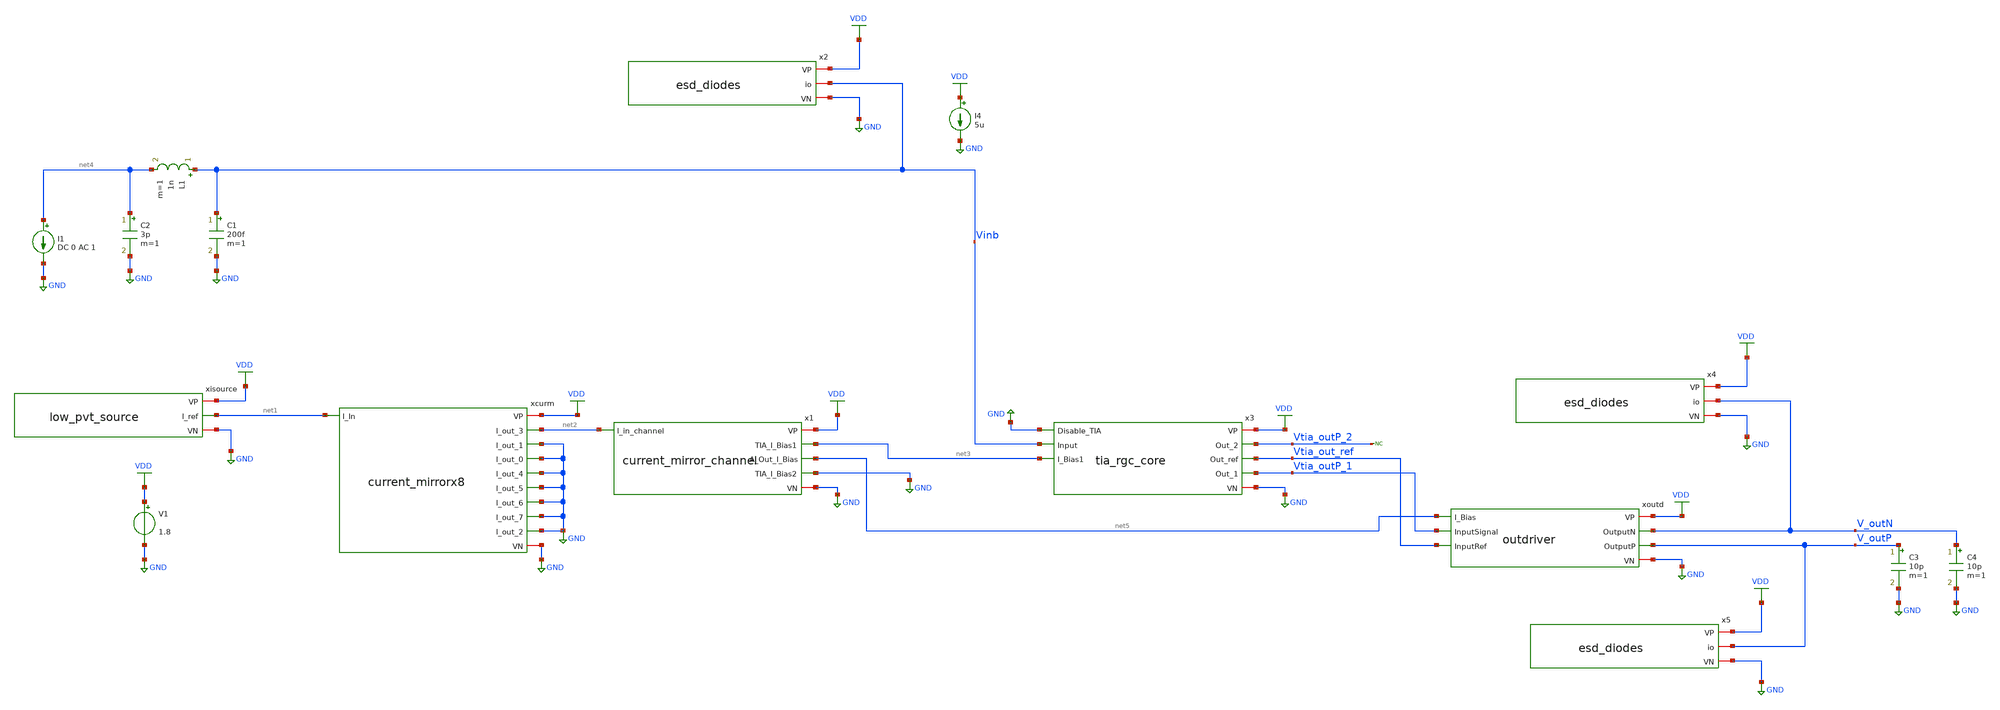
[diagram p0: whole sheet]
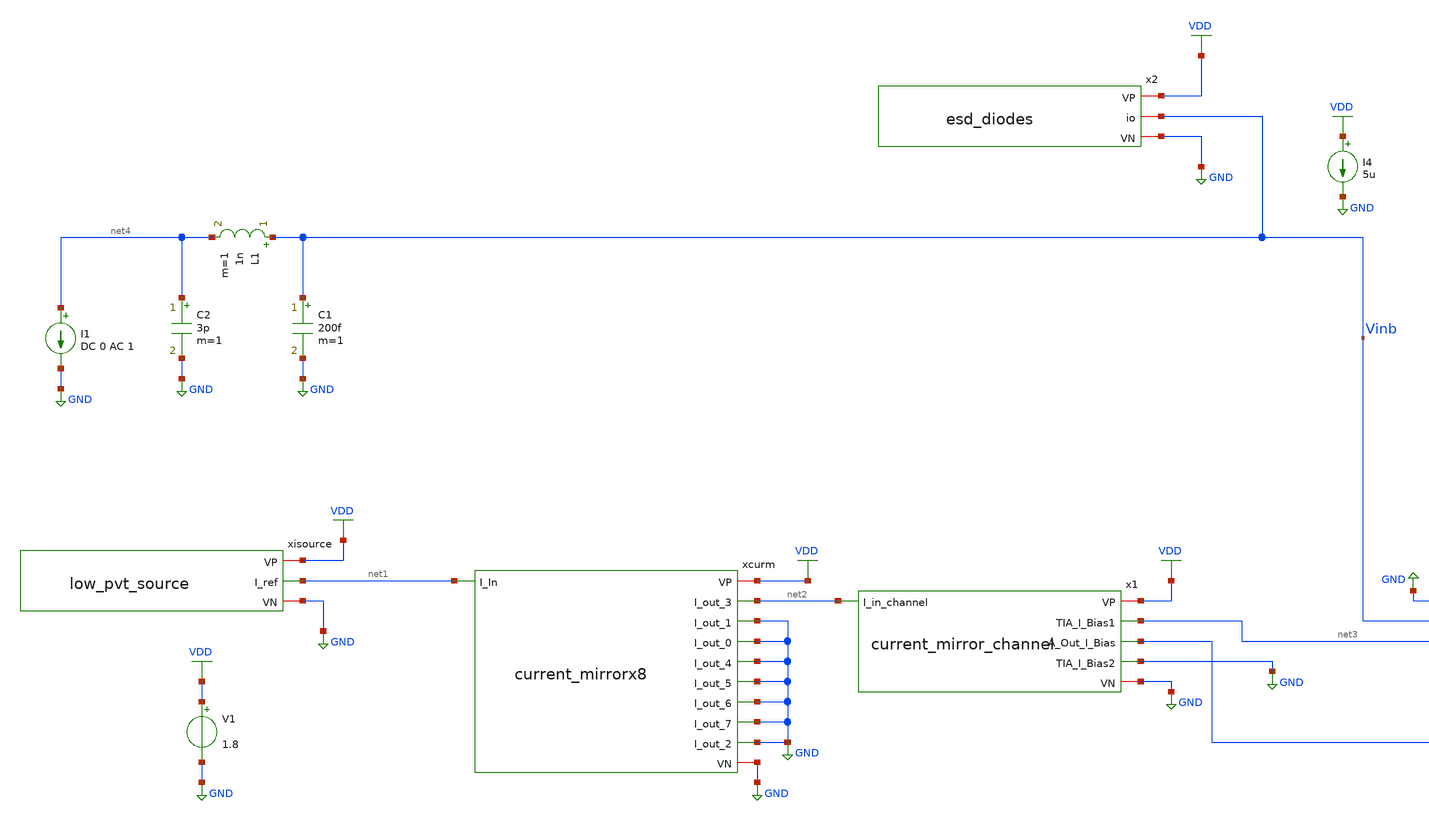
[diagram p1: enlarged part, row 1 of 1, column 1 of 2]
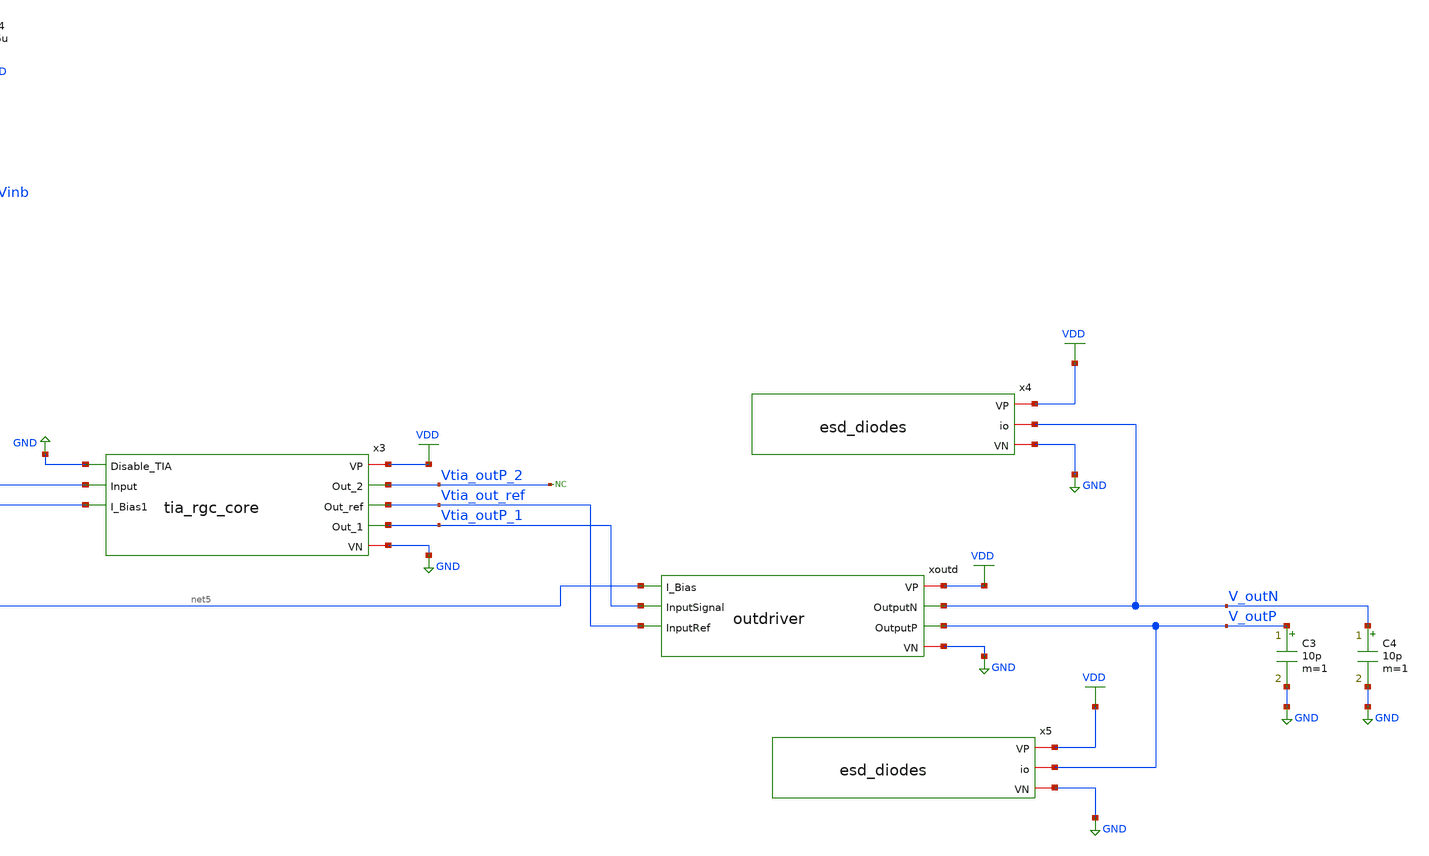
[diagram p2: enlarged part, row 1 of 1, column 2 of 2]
** sch_path: xschem/test/test_tia_rgc_integration.sch
**.subckt test_tia_rgc_integration
xcurm VDD net2 GND net1 GND GND GND GND GND GND GND current_mirrorx8
xisource VDD net1 GND low_pvt_source
x1 VDD net3 net5 GND net2 GND current_mirror_channel
V1 VDD GND 1.8
I1 net4 GND DC 0 AC 1
C1 Vinb GND 200f m=1
L1 Vinb net4 1n m=1
C2 net4 GND 3p m=1
I4 VDD GND 5u
* noconn Vtia_outP_2
xoutd VDD V_outN V_outP net5 Vtia_outP_1 Vtia_out_ref GND outdriver
x3 VDD Vtia_outP_2 Vtia_out_ref Vtia_outP_1 GND Vinb net3 GND tia_rgc_core
C3 V_outP GND 10p m=1
C4 V_outN GND 10p m=1
x2 VDD Vinb GND esd_diodes
x4 VDD V_outN GND esd_diodes
x5 VDD V_outP GND esd_diodes
**** begin user architecture code


*.options savecurrents
.option warn=1
* .option temp=100
.control
set wr_vecnames
set wr_singlescale
set hcopydevtype=svg
** TIA


op
write test_tia_rgc_integration.raw
run
reset

ac dec 1000 10 1T
plot vdb(Vtia_outP_1) vdb(Vtia_outP_2)
plot v(Vinb)
plot phase(Vinb)/pi*180 phase(Vtia_outP_1)/pi*180

plot db(v(V_outP)-v(V_outN))

* tran 1p 100n
* plot v(Vtia_outP_1) v(Vtia_outP_2)
* plot v(Vinb)

meas ac gain FIND vdb(vtia_outp_1) AT=10MEG
meas ac max_gain max vdb(vtia_outp_1) from=1MEG to=100G
meas ac min_gain min vdb(vtia_outp_1) from=1MEG to=100MEG
let bw_gain=gain-3
meas ac bandwidth when vdb(vtia_outp_1)=bw_gain fall = LAST
wrdata result_ac_tia.csv gain max_gain min_gain bandwidth


noise v(vtia_outp_1) i1 dec 1000 10 2G
print all
* wrdata result_noise.csv inoise_total onoise_total
setplot noise1
plot inoise_spectrum
plot onoise_spectrum
* hardcopy tia_rgc_inoise_spectrum.svg inoise_spectrum
* hardcopy tia_rgc_onoise_spectrum.svg onoise_spectrum
* plot log(inoise_spectrum)
* write noise_tia2.raw

noise v(vtia_outp_1) i1 dec 1000 2MEG 2G
print all
* wrdata result_noise.csv inoise_total onoise_total
setplot noise3
plot inoise_spectrum
plot onoise_spectrum
* hardcopy tia_rgc_inoise_spectrum_zoom.svg inoise_spectrum
* hardcopy tia_rgc_onoise_spectrum_zoom.svg onoise_spectrum
* plot log(inoise_spectrum)
* write noise_tia2.raw

noise v(v_outp) i1 dec 1000 2MEG 2G
print all
setplot noise5
plot inoise_spectrum
plot onoise_spectrum

noise v(v_outp) i1 dec 1000 10 2G
print all
setplot noise7
plot inoise_spectrum
plot onoise_spectrum


.endc




* .include ../../tia.spice
* .include ../../filter_diff.spice
* .include ../../cmm_sense3.spice

.include tia_rgc_core.spice
.include current_mirror_channel.spice
.include current_mirrorx8.spice
.include low_pvt_source.spice
.include outdriver.spice
.include esd_diodes.spice



* .lib $::SKYWATER_MODELS/sky130.lib.spice #model#
* .lib $::SKYWATER_MODELS/sky130.lib.spice sf
.lib $::SKYWATER_MODELS/sky130.lib.spice.ll.red ll
* .lib /home/simon/share/pdk/sky130A/libs.tech/ngspice/sky130.lib.spice.tt.red tt

**** end user architecture code
**.ends

* expanding   symbol:  /home/simon/code/asic/analog/bias/current_mirrorx8.sym # of pins=11
** sym_path: xschem/bias/current_mirrorx8.sym
** sch_path: xschem/bias/current_mirrorx8.sch
.subckt current_mirrorx8 VP I_out_3 I_out_1 I_In I_out_0 I_out_4 I_out_5 I_out_6 I_out_7 I_out_2 VN
*.opin I_out_0
*.ipin I_In
*.iopin VP
*.opin I_out_1
*.opin I_out_2
*.opin I_out_3
*.opin I_out_4
*.opin I_out_5
*.opin I_out_6
*.opin I_out_7
*.iopin VN
XM1 net1 I_In VP VP sky130_fd_pr__pfet_01v8 L=1 W=2 nf=1 ad='int((nf+1)/2) * W/nf * 0.29' as='int((nf+2)/2) * W/nf * 0.29'
+ pd='2*int((nf+1)/2) * (W/nf + 0.29)' ps='2*int((nf+2)/2) * (W/nf + 0.29)' nrd='0.29 / W' nrs='0.29 / W'
+ sa=0 sb=0 sd=0 mult=4*4 m=4*4
XM2 I_In I_In net1 VP sky130_fd_pr__pfet_01v8 L=0.2 W=2 nf=1 ad='int((nf+1)/2) * W/nf * 0.29' as='int((nf+2)/2) * W/nf * 0.29'
+ pd='2*int((nf+1)/2) * (W/nf + 0.29)' ps='2*int((nf+2)/2) * (W/nf + 0.29)' nrd='0.29 / W' nrs='0.29 / W'
+ sa=0 sb=0 sd=0 mult=4 m=4
XC1 I_In VP sky130_fd_pr__cap_mim_m3_1 W=20 L=20 MF=1 m=1
XC2 VP I_In sky130_fd_pr__cap_mim_m3_2 W=20 L=20 MF=1 m=1
XC4 VP VN VN sky130_fd_pr__cap_var_lvt W=2 L=5 VM=5 m=5
XC3 I_In VN VN sky130_fd_pr__cap_var_lvt W=2 L=5 VM=5 m=5
XM3 net2 I_In VP VP sky130_fd_pr__pfet_01v8 L=1 W=2 nf=1 ad='int((nf+1)/2) * W/nf * 0.29' as='int((nf+2)/2) * W/nf * 0.29'
+ pd='2*int((nf+1)/2) * (W/nf + 0.29)' ps='2*int((nf+2)/2) * (W/nf + 0.29)' nrd='0.29 / W' nrs='0.29 / W'
+ sa=0 sb=0 sd=0 mult=4*4 m=4*4
XM4 I_out_0 I_In net2 VP sky130_fd_pr__pfet_01v8 L=0.2 W=2 nf=1 ad='int((nf+1)/2) * W/nf * 0.29' as='int((nf+2)/2) * W/nf * 0.29'
+ pd='2*int((nf+1)/2) * (W/nf + 0.29)' ps='2*int((nf+2)/2) * (W/nf + 0.29)' nrd='0.29 / W' nrs='0.29 / W'
+ sa=0 sb=0 sd=0 mult=4 m=4
XM5 net3 I_In VP VP sky130_fd_pr__pfet_01v8 L=1 W=2 nf=1 ad='int((nf+1)/2) * W/nf * 0.29' as='int((nf+2)/2) * W/nf * 0.29'
+ pd='2*int((nf+1)/2) * (W/nf + 0.29)' ps='2*int((nf+2)/2) * (W/nf + 0.29)' nrd='0.29 / W' nrs='0.29 / W'
+ sa=0 sb=0 sd=0 mult=4*4 m=4*4
XM6 I_out_1 I_In net3 VP sky130_fd_pr__pfet_01v8 L=0.2 W=2 nf=1 ad='int((nf+1)/2) * W/nf * 0.29' as='int((nf+2)/2) * W/nf * 0.29'
+ pd='2*int((nf+1)/2) * (W/nf + 0.29)' ps='2*int((nf+2)/2) * (W/nf + 0.29)' nrd='0.29 / W' nrs='0.29 / W'
+ sa=0 sb=0 sd=0 mult=4 m=4
XM7 net4 I_In VP VP sky130_fd_pr__pfet_01v8 L=1 W=2 nf=1 ad='int((nf+1)/2) * W/nf * 0.29' as='int((nf+2)/2) * W/nf * 0.29'
+ pd='2*int((nf+1)/2) * (W/nf + 0.29)' ps='2*int((nf+2)/2) * (W/nf + 0.29)' nrd='0.29 / W' nrs='0.29 / W'
+ sa=0 sb=0 sd=0 mult=4*4 m=4*4
XM8 I_out_2 I_In net4 VP sky130_fd_pr__pfet_01v8 L=0.2 W=2 nf=1 ad='int((nf+1)/2) * W/nf * 0.29' as='int((nf+2)/2) * W/nf * 0.29'
+ pd='2*int((nf+1)/2) * (W/nf + 0.29)' ps='2*int((nf+2)/2) * (W/nf + 0.29)' nrd='0.29 / W' nrs='0.29 / W'
+ sa=0 sb=0 sd=0 mult=4 m=4
XM9 net5 I_In VP VP sky130_fd_pr__pfet_01v8 L=1 W=2 nf=1 ad='int((nf+1)/2) * W/nf * 0.29' as='int((nf+2)/2) * W/nf * 0.29'
+ pd='2*int((nf+1)/2) * (W/nf + 0.29)' ps='2*int((nf+2)/2) * (W/nf + 0.29)' nrd='0.29 / W' nrs='0.29 / W'
+ sa=0 sb=0 sd=0 mult=4*4 m=4*4
XM10 I_out_3 I_In net5 VP sky130_fd_pr__pfet_01v8 L=0.2 W=2 nf=1 ad='int((nf+1)/2) * W/nf * 0.29' as='int((nf+2)/2) * W/nf * 0.29'
+ pd='2*int((nf+1)/2) * (W/nf + 0.29)' ps='2*int((nf+2)/2) * (W/nf + 0.29)' nrd='0.29 / W' nrs='0.29 / W'
+ sa=0 sb=0 sd=0 mult=4 m=4
XM11 net6 I_In VP VP sky130_fd_pr__pfet_01v8 L=1 W=2 nf=1 ad='int((nf+1)/2) * W/nf * 0.29' as='int((nf+2)/2) * W/nf * 0.29'
+ pd='2*int((nf+1)/2) * (W/nf + 0.29)' ps='2*int((nf+2)/2) * (W/nf + 0.29)' nrd='0.29 / W' nrs='0.29 / W'
+ sa=0 sb=0 sd=0 mult=4*4 m=4*4
XM12 I_out_4 I_In net6 VP sky130_fd_pr__pfet_01v8 L=0.2 W=2 nf=1 ad='int((nf+1)/2) * W/nf * 0.29' as='int((nf+2)/2) * W/nf * 0.29'
+ pd='2*int((nf+1)/2) * (W/nf + 0.29)' ps='2*int((nf+2)/2) * (W/nf + 0.29)' nrd='0.29 / W' nrs='0.29 / W'
+ sa=0 sb=0 sd=0 mult=4 m=4
XM13 net7 I_In VP VP sky130_fd_pr__pfet_01v8 L=1 W=2 nf=1 ad='int((nf+1)/2) * W/nf * 0.29' as='int((nf+2)/2) * W/nf * 0.29'
+ pd='2*int((nf+1)/2) * (W/nf + 0.29)' ps='2*int((nf+2)/2) * (W/nf + 0.29)' nrd='0.29 / W' nrs='0.29 / W'
+ sa=0 sb=0 sd=0 mult=4*4 m=4*4
XM14 I_out_5 I_In net7 VP sky130_fd_pr__pfet_01v8 L=0.2 W=2 nf=1 ad='int((nf+1)/2) * W/nf * 0.29' as='int((nf+2)/2) * W/nf * 0.29'
+ pd='2*int((nf+1)/2) * (W/nf + 0.29)' ps='2*int((nf+2)/2) * (W/nf + 0.29)' nrd='0.29 / W' nrs='0.29 / W'
+ sa=0 sb=0 sd=0 mult=4 m=4
XM15 net8 I_In VP VP sky130_fd_pr__pfet_01v8 L=1 W=2 nf=1 ad='int((nf+1)/2) * W/nf * 0.29' as='int((nf+2)/2) * W/nf * 0.29'
+ pd='2*int((nf+1)/2) * (W/nf + 0.29)' ps='2*int((nf+2)/2) * (W/nf + 0.29)' nrd='0.29 / W' nrs='0.29 / W'
+ sa=0 sb=0 sd=0 mult=4*4 m=4*4
XM16 I_out_6 I_In net8 VP sky130_fd_pr__pfet_01v8 L=0.2 W=2 nf=1 ad='int((nf+1)/2) * W/nf * 0.29' as='int((nf+2)/2) * W/nf * 0.29'
+ pd='2*int((nf+1)/2) * (W/nf + 0.29)' ps='2*int((nf+2)/2) * (W/nf + 0.29)' nrd='0.29 / W' nrs='0.29 / W'
+ sa=0 sb=0 sd=0 mult=4 m=4
XM17 net9 I_In VP VP sky130_fd_pr__pfet_01v8 L=1 W=2 nf=1 ad='int((nf+1)/2) * W/nf * 0.29' as='int((nf+2)/2) * W/nf * 0.29'
+ pd='2*int((nf+1)/2) * (W/nf + 0.29)' ps='2*int((nf+2)/2) * (W/nf + 0.29)' nrd='0.29 / W' nrs='0.29 / W'
+ sa=0 sb=0 sd=0 mult=4*4 m=4*4
XM18 I_out_7 I_In net9 VP sky130_fd_pr__pfet_01v8 L=0.2 W=2 nf=1 ad='int((nf+1)/2) * W/nf * 0.29' as='int((nf+2)/2) * W/nf * 0.29'
+ pd='2*int((nf+1)/2) * (W/nf + 0.29)' ps='2*int((nf+2)/2) * (W/nf + 0.29)' nrd='0.29 / W' nrs='0.29 / W'
+ sa=0 sb=0 sd=0 mult=4 m=4
.ends


* expanding   symbol:  /home/simon/code/asic/analog/bias/low_pvt_source.sym # of pins=3
** sym_path: xschem/bias/low_pvt_source.sym
** sch_path: xschem/bias/low_pvt_source.sch
.subckt low_pvt_source VP I_ref VN
*.iopin VP
*.opin I_ref
*.iopin VN
XM1 VM1D VM8D VP VP sky130_fd_pr__pfet_01v8 L=1 W=4 nf=1 ad='int((nf+1)/2) * W/nf * 0.29' as='int((nf+2)/2) * W/nf * 0.29'
+ pd='2*int((nf+1)/2) * (W/nf + 0.29)' ps='2*int((nf+2)/2) * (W/nf + 0.29)' nrd='0.29 / W' nrs='0.29 / W'
+ sa=0 sb=0 sd=0 mult=10 m=10
XM2 VM2D VM2D VN VN sky130_fd_pr__nfet_01v8 L=6 W=4 nf=1 ad='int((nf+1)/2) * W/nf * 0.29' as='int((nf+2)/2) * W/nf * 0.29'
+ pd='2*int((nf+1)/2) * (W/nf + 0.29)' ps='2*int((nf+2)/2) * (W/nf + 0.29)' nrd='0.29 / W' nrs='0.29 / W'
+ sa=0 sb=0 sd=0 mult=30 m=30
XM5 VM9D VM8D VM1D VP sky130_fd_pr__pfet_01v8 L=0.2 W=4 nf=1 ad='int((nf+1)/2) * W/nf * 0.29' as='int((nf+2)/2) * W/nf * 0.29'
+ pd='2*int((nf+1)/2) * (W/nf + 0.29)' ps='2*int((nf+2)/2) * (W/nf + 0.29)' nrd='0.29 / W' nrs='0.29 / W'
+ sa=0 sb=0 sd=0 mult=2 m=2
XM11 VM11D VM2D VM12D VN sky130_fd_pr__nfet_01v8 L=6 W=4 nf=1 ad='int((nf+1)/2) * W/nf * 0.29' as='int((nf+2)/2) * W/nf * 0.29'
+ pd='2*int((nf+1)/2) * (W/nf + 0.29)' ps='2*int((nf+2)/2) * (W/nf + 0.29)' nrd='0.29 / W' nrs='0.29 / W'
+ sa=0 sb=0 sd=0 mult=65 m=65
XM12 VM12D VM12G VN VN sky130_fd_pr__nfet_01v8 L=6 W=4 nf=1 ad='int((nf+1)/2) * W/nf * 0.29' as='int((nf+2)/2) * W/nf * 0.29'
+ pd='2*int((nf+1)/2) * (W/nf + 0.29)' ps='2*int((nf+2)/2) * (W/nf + 0.29)' nrd='0.29 / W' nrs='0.29 / W'
+ sa=0 sb=0 sd=0 mult=2 m=2
XM14 VM14D VM12G VN VN sky130_fd_pr__nfet_01v8 L=6 W=4 nf=1 ad='int((nf+1)/2) * W/nf * 0.29' as='int((nf+2)/2) * W/nf * 0.29'
+ pd='2*int((nf+1)/2) * (W/nf + 0.29)' ps='2*int((nf+2)/2) * (W/nf + 0.29)' nrd='0.29 / W' nrs='0.29 / W'
+ sa=0 sb=0 sd=0 mult=2 m=2
XM16 VM16D VM8D VP VP sky130_fd_pr__pfet_01v8 L=1 W=4 nf=1 ad='int((nf+1)/2) * W/nf * 0.29' as='int((nf+2)/2) * W/nf * 0.29'
+ pd='2*int((nf+1)/2) * (W/nf + 0.29)' ps='2*int((nf+2)/2) * (W/nf + 0.29)' nrd='0.29 / W' nrs='0.29 / W'
+ sa=0 sb=0 sd=0 mult=10 m=10
XM17 VM8D VM8D VM16D VP sky130_fd_pr__pfet_01v8 L=0.2 W=4 nf=1 ad='int((nf+1)/2) * W/nf * 0.29' as='int((nf+2)/2) * W/nf * 0.29'
+ pd='2*int((nf+1)/2) * (W/nf + 0.29)' ps='2*int((nf+2)/2) * (W/nf + 0.29)' nrd='0.29 / W' nrs='0.29 / W'
+ sa=0 sb=0 sd=0 mult=2 m=2
XM18 VM18D VM8D VP VP sky130_fd_pr__pfet_01v8 L=1 W=4 nf=1 ad='int((nf+1)/2) * W/nf * 0.29' as='int((nf+2)/2) * W/nf * 0.29'
+ pd='2*int((nf+1)/2) * (W/nf + 0.29)' ps='2*int((nf+2)/2) * (W/nf + 0.29)' nrd='0.29 / W' nrs='0.29 / W'
+ sa=0 sb=0 sd=0 mult=10*3*2 m=10*3*2
XM19 VM14D VM8D VM18D VP sky130_fd_pr__pfet_01v8 L=0.2 W=4 nf=1 ad='int((nf+1)/2) * W/nf * 0.29' as='int((nf+2)/2) * W/nf * 0.29'
+ pd='2*int((nf+1)/2) * (W/nf + 0.29)' ps='2*int((nf+2)/2) * (W/nf + 0.29)' nrd='0.29 / W' nrs='0.29 / W'
+ sa=0 sb=0 sd=0 mult=2*3*2 m=2*3*2
XM20 VM20D VM8D VP VP sky130_fd_pr__pfet_01v8 L=1 W=4 nf=1 ad='int((nf+1)/2) * W/nf * 0.29' as='int((nf+2)/2) * W/nf * 0.29'
+ pd='2*int((nf+1)/2) * (W/nf + 0.29)' ps='2*int((nf+2)/2) * (W/nf + 0.29)' nrd='0.29 / W' nrs='0.29 / W'
+ sa=0 sb=0 sd=0 mult=10*1*1 m=10*1*1
XM21 VM22D VM8D VM20D VP sky130_fd_pr__pfet_01v8 L=0.2 W=4 nf=1 ad='int((nf+1)/2) * W/nf * 0.29' as='int((nf+2)/2) * W/nf * 0.29'
+ pd='2*int((nf+1)/2) * (W/nf + 0.29)' ps='2*int((nf+2)/2) * (W/nf + 0.29)' nrd='0.29 / W' nrs='0.29 / W'
+ sa=0 sb=0 sd=0 mult=2*1*1 m=2*1*1
XM22 VM22D VM4S VM3D VN sky130_fd_pr__nfet_01v8 L=6 W=4 nf=1 ad='int((nf+1)/2) * W/nf * 0.29' as='int((nf+2)/2) * W/nf * 0.29'
+ pd='2*int((nf+1)/2) * (W/nf + 0.29)' ps='2*int((nf+2)/2) * (W/nf + 0.29)' nrd='0.29 / W' nrs='0.29 / W'
+ sa=0 sb=0 sd=0 mult=20 m=20
XM3 VM3D VM3G VN VN sky130_fd_pr__nfet_01v8 L=6 W=4 nf=1 ad='int((nf+1)/2) * W/nf * 0.29' as='int((nf+2)/2) * W/nf * 0.29'
+ pd='2*int((nf+1)/2) * (W/nf + 0.29)' ps='2*int((nf+2)/2) * (W/nf + 0.29)' nrd='0.29 / W' nrs='0.29 / W'
+ sa=0 sb=0 sd=0 mult=4 m=4
XM13 VP VM14D VM12G VM12G sky130_fd_pr__nfet_01v8_lvt L=0.15 W=4 nf=1 ad='int((nf+1)/2) * W/nf * 0.29'
+ as='int((nf+2)/2) * W/nf * 0.29' pd='2*int((nf+1)/2) * (W/nf + 0.29)' ps='2*int((nf+2)/2) * (W/nf + 0.29)'
+ nrd='0.29 / W' nrs='0.29 / W' sa=0 sb=0 sd=0 mult=20 m=20
XM4 I_ref VM22D VM4S VN sky130_fd_pr__nfet_01v8_lvt L=0.15 W=4 nf=1 ad='int((nf+1)/2) * W/nf * 0.29'
+ as='int((nf+2)/2) * W/nf * 0.29' pd='2*int((nf+1)/2) * (W/nf + 0.29)' ps='2*int((nf+2)/2) * (W/nf + 0.29)'
+ nrd='0.29 / W' nrs='0.29 / W' sa=0 sb=0 sd=0 mult=20 m=20
XM48 VM50D VM11D VP VP sky130_fd_pr__pfet_01v8 L=2 W=0.5 nf=1 ad='int((nf+1)/2) * W/nf * 0.29' as='int((nf+2)/2) * W/nf * 0.29'
+ pd='2*int((nf+1)/2) * (W/nf + 0.29)' ps='2*int((nf+2)/2) * (W/nf + 0.29)' nrd='0.29 / W' nrs='0.29 / W'
+ sa=0 sb=0 sd=0 mult=1 m=1
XM50 VM50D VM11D VN VN sky130_fd_pr__nfet_01v8_lvt L=0.2 W=4 nf=1 ad='int((nf+1)/2) * W/nf * 0.29' as='int((nf+2)/2) * W/nf * 0.29'
+ pd='2*int((nf+1)/2) * (W/nf + 0.29)' ps='2*int((nf+2)/2) * (W/nf + 0.29)' nrd='0.29 / W' nrs='0.29 / W'
+ sa=0 sb=0 sd=0 mult=10 m=10
XC3 VP VM8D sky130_fd_pr__cap_mim_m3_1 W=20 L=20 MF=1 m=1
XM8 VM8D VM9D VM11D VM11D sky130_fd_pr__nfet_01v8_lvt L=1 W=4 nf=1 ad='int((nf+1)/2) * W/nf * 0.29' as='int((nf+2)/2) * W/nf * 0.29'
+ pd='2*int((nf+1)/2) * (W/nf + 0.29)' ps='2*int((nf+2)/2) * (W/nf + 0.29)' nrd='0.29 / W' nrs='0.29 / W'
+ sa=0 sb=0 sd=0 mult=20 m=20
XM9 VM9D VM9D VM2D VM2D sky130_fd_pr__nfet_01v8_lvt L=1 W=4 nf=1 ad='int((nf+1)/2) * W/nf * 0.29' as='int((nf+2)/2) * W/nf * 0.29'
+ pd='2*int((nf+1)/2) * (W/nf + 0.29)' ps='2*int((nf+2)/2) * (W/nf + 0.29)' nrd='0.29 / W' nrs='0.29 / W'
+ sa=0 sb=0 sd=0 mult=20 m=20
XM10 VM8D VM50D VN VN sky130_fd_pr__nfet_01v8 L=2 W=0.5 nf=1 ad='int((nf+1)/2) * W/nf * 0.29' as='int((nf+2)/2) * W/nf * 0.29'
+ pd='2*int((nf+1)/2) * (W/nf + 0.29)' ps='2*int((nf+2)/2) * (W/nf + 0.29)' nrd='0.29 / W' nrs='0.29 / W'
+ sa=0 sb=0 sd=0 mult=1 m=1
XC4 VN VP sky130_fd_pr__cap_mim_m3_2 W=30 L=30 MF=1 m=1
XR7 net3 VM4S VN sky130_fd_pr__res_xhigh_po_1p41 L=10 mult=1 m=1
XR3 net4 net3 VN sky130_fd_pr__res_xhigh_po_1p41 L=10 mult=1 m=1
XR4 net2 net4 VN sky130_fd_pr__res_xhigh_po_1p41 L=10 mult=1 m=1
XR5 net1 net2 VN sky130_fd_pr__res_xhigh_po_1p41 L=10 mult=1 m=1
XR6 VN net1 VN sky130_fd_pr__res_xhigh_po_1p41 L=10 mult=1 m=1
XR8 net5 VM12G VN sky130_fd_pr__res_xhigh_po_1p41 L=10 mult=1 m=1
XR1 net5 VM3G VN sky130_fd_pr__res_xhigh_po_1p41 L=10 mult=1 m=1
XR2 net7 net6 VN sky130_fd_pr__res_xhigh_po_1p41 L=10 mult=1 m=1
XR9 VN net6 VN sky130_fd_pr__res_xhigh_po_1p41 L=10 mult=1 m=1
XR10 net11 net7 VN sky130_fd_pr__res_xhigh_po_1p41 L=10 mult=1 m=1
XR11 net12 net11 VN sky130_fd_pr__res_xhigh_po_1p41 L=10 mult=1 m=1
XR12 net8 net12 VN sky130_fd_pr__res_xhigh_po_1p41 L=10 mult=1 m=1
XR13 net10 VM3G VN sky130_fd_pr__res_xhigh_po_1p41 L=10 mult=1 m=1
XR14 net9 net10 VN sky130_fd_pr__res_xhigh_po_1p41 L=10 mult=1 m=1
XR15 net8 net9 VN sky130_fd_pr__res_xhigh_po_1p41 L=10 mult=1 m=1
XC1 VN VP sky130_fd_pr__cap_mim_m3_2 W=30 L=30 MF=1 m=1
.ends


* expanding   symbol:  /home/simon/code/asic/analog/bias/current_mirror_channel.sym # of pins=6
** sym_path: xschem/bias/current_mirror_channel.sym
** sch_path: xschem/bias/current_mirror_channel.sch
.subckt current_mirror_channel VP TIA_I_Bias1 A_Out_I_Bias TIA_I_Bias2 I_in_channel VN
*.ipin I_in_channel
*.iopin VP
*.opin TIA_I_Bias2
*.iopin VN
*.opin TIA_I_Bias1
*.opin A_Out_I_Bias
XM1 I_in_channel I_in_channel net1 VN sky130_fd_pr__nfet_01v8 L=0.2 W=2 nf=1 ad='int((nf+1)/2) * W/nf * 0.29'
+ as='int((nf+2)/2) * W/nf * 0.29' pd='2*int((nf+1)/2) * (W/nf + 0.29)' ps='2*int((nf+2)/2) * (W/nf + 0.29)'
+ nrd='0.29 / W' nrs='0.29 / W' sa=0 sb=0 sd=0 mult=2 m=2
XM2 net5 net4 VP VP sky130_fd_pr__pfet_01v8 L=1 W=2 nf=1 ad='int((nf+1)/2) * W/nf * 0.29' as='int((nf+2)/2) * W/nf * 0.29'
+ pd='2*int((nf+1)/2) * (W/nf + 0.29)' ps='2*int((nf+2)/2) * (W/nf + 0.29)' nrd='0.29 / W' nrs='0.29 / W'
+ sa=0 sb=0 sd=0 mult=4*4 m=4*4
XM3 net1 I_in_channel VN VN sky130_fd_pr__nfet_01v8 L=1 W=2 nf=1 ad='int((nf+1)/2) * W/nf * 0.29' as='int((nf+2)/2) * W/nf * 0.29'
+ pd='2*int((nf+1)/2) * (W/nf + 0.29)' ps='2*int((nf+2)/2) * (W/nf + 0.29)' nrd='0.29 / W' nrs='0.29 / W'
+ sa=0 sb=0 sd=0 mult=2*4 m=2*4
XM4 net4 net4 net5 VP sky130_fd_pr__pfet_01v8 L=0.2 W=2 nf=1 ad='int((nf+1)/2) * W/nf * 0.29' as='int((nf+2)/2) * W/nf * 0.29'
+ pd='2*int((nf+1)/2) * (W/nf + 0.29)' ps='2*int((nf+2)/2) * (W/nf + 0.29)' nrd='0.29 / W' nrs='0.29 / W'
+ sa=0 sb=0 sd=0 mult=4 m=4
XC8 net4 VP sky130_fd_pr__cap_mim_m3_2 W=30 L=30 MF=1 m=1
XM5 net4 I_in_channel net2 VN sky130_fd_pr__nfet_01v8 L=0.2 W=2 nf=1 ad='int((nf+1)/2) * W/nf * 0.29'
+ as='int((nf+2)/2) * W/nf * 0.29' pd='2*int((nf+1)/2) * (W/nf + 0.29)' ps='2*int((nf+2)/2) * (W/nf + 0.29)'
+ nrd='0.29 / W' nrs='0.29 / W' sa=0 sb=0 sd=0 mult=2 m=2
XM6 TIA_I_Bias2 I_in_channel net3 VN sky130_fd_pr__nfet_01v8 L=0.2 W=2 nf=1 ad='int((nf+1)/2) * W/nf * 0.29'
+ as='int((nf+2)/2) * W/nf * 0.29' pd='2*int((nf+1)/2) * (W/nf + 0.29)' ps='2*int((nf+2)/2) * (W/nf + 0.29)'
+ nrd='0.29 / W' nrs='0.29 / W' sa=0 sb=0 sd=0 mult=2 m=2
XM7 net2 I_in_channel VN VN sky130_fd_pr__nfet_01v8 L=1 W=2 nf=1 ad='int((nf+1)/2) * W/nf * 0.29' as='int((nf+2)/2) * W/nf * 0.29'
+ pd='2*int((nf+1)/2) * (W/nf + 0.29)' ps='2*int((nf+2)/2) * (W/nf + 0.29)' nrd='0.29 / W' nrs='0.29 / W'
+ sa=0 sb=0 sd=0 mult=2*4 m=2*4
XM8 net3 I_in_channel VN VN sky130_fd_pr__nfet_01v8 L=1 W=2 nf=1 ad='int((nf+1)/2) * W/nf * 0.29' as='int((nf+2)/2) * W/nf * 0.29'
+ pd='2*int((nf+1)/2) * (W/nf + 0.29)' ps='2*int((nf+2)/2) * (W/nf + 0.29)' nrd='0.29 / W' nrs='0.29 / W'
+ sa=0 sb=0 sd=0 mult=2*4 m=2*4
XM13 net6 net4 VP VP sky130_fd_pr__pfet_01v8 L=1 W=2 nf=1 ad='int((nf+1)/2) * W/nf * 0.29' as='int((nf+2)/2) * W/nf * 0.29'
+ pd='2*int((nf+1)/2) * (W/nf + 0.29)' ps='2*int((nf+2)/2) * (W/nf + 0.29)' nrd='0.29 / W' nrs='0.29 / W'
+ sa=0 sb=0 sd=0 mult=4*4*10 m=4*4*10
XM14 TIA_I_Bias1 net4 net6 VP sky130_fd_pr__pfet_01v8 L=0.2 W=2 nf=1 ad='int((nf+1)/2) * W/nf * 0.29'
+ as='int((nf+2)/2) * W/nf * 0.29' pd='2*int((nf+1)/2) * (W/nf + 0.29)' ps='2*int((nf+2)/2) * (W/nf + 0.29)'
+ nrd='0.29 / W' nrs='0.29 / W' sa=0 sb=0 sd=0 mult=4*10 m=4*10
XM9 net7 net4 VP VP sky130_fd_pr__pfet_01v8 L=1 W=2 nf=1 ad='int((nf+1)/2) * W/nf * 0.29' as='int((nf+2)/2) * W/nf * 0.29'
+ pd='2*int((nf+1)/2) * (W/nf + 0.29)' ps='2*int((nf+2)/2) * (W/nf + 0.29)' nrd='0.29 / W' nrs='0.29 / W'
+ sa=0 sb=0 sd=0 mult=4*4*12 m=4*4*12
XM10 A_Out_I_Bias net4 net7 VP sky130_fd_pr__pfet_01v8 L=0.2 W=2 nf=1 ad='int((nf+1)/2) * W/nf * 0.29'
+ as='int((nf+2)/2) * W/nf * 0.29' pd='2*int((nf+1)/2) * (W/nf + 0.29)' ps='2*int((nf+2)/2) * (W/nf + 0.29)'
+ nrd='0.29 / W' nrs='0.29 / W' sa=0 sb=0 sd=0 mult=4*12 m=4*12
XC4 net4 VP sky130_fd_pr__cap_mim_m3_2 W=30 L=30 MF=1 m=1
XC3 VN I_in_channel sky130_fd_pr__cap_mim_m3_2 W=30 L=30 MF=1 m=1
XC6 VN I_in_channel sky130_fd_pr__cap_mim_m3_2 W=30 L=30 MF=1 m=1
XC1 VN net4 sky130_fd_pr__cap_mim_m3_2 W=30 L=30 MF=1 m=1
XC2 VN VP sky130_fd_pr__cap_mim_m3_2 W=30 L=30 MF=1 m=1
.ends


* expanding   symbol:  /home/simon/code/asic/analog/outdriver/outdriver.sym # of pins=7
** sym_path: xschem/outdriver/outdriver.sym
** sch_path: xschem/outdriver/outdriver.sch
.subckt outdriver VP OutputN OutputP I_Bias InputSignal InputRef VN
*.iopin VN
*.ipin InputRef
*.iopin VP
*.ipin I_Bias
*.ipin InputSignal
*.opin OutputN
*.opin OutputP
XM1 V_da1_P InputSignal VM6D VM6D sky130_fd_pr__nfet_01v8_lvt L=0.15 W=2 nf=1 ad='int((nf+1)/2) * W/nf * 0.29'
+ as='int((nf+2)/2) * W/nf * 0.29' pd='2*int((nf+1)/2) * (W/nf + 0.29)' ps='2*int((nf+2)/2) * (W/nf + 0.29)'
+ nrd='0.29 / W' nrs='0.29 / W' sa=0 sb=0 sd=0 mult=11*2 m=11*2
XM3 VM3D I_Bias net4 VN sky130_fd_pr__nfet_01v8 L=0.5 W=2 nf=1 ad='int((nf+1)/2) * W/nf * 0.29' as='int((nf+2)/2) * W/nf * 0.29'
+ pd='2*int((nf+1)/2) * (W/nf + 0.29)' ps='2*int((nf+2)/2) * (W/nf + 0.29)' nrd='0.29 / W' nrs='0.29 / W'
+ sa=0 sb=0 sd=0 mult=2*(64) m=2*(64)
XM6 VM6D I_Bias VM3D VN sky130_fd_pr__nfet_01v8 L=0.15 W=2 nf=1 ad='int((nf+1)/2) * W/nf * 0.29' as='int((nf+2)/2) * W/nf * 0.29'
+ pd='2*int((nf+1)/2) * (W/nf + 0.29)' ps='2*int((nf+2)/2) * (W/nf + 0.29)' nrd='0.29 / W' nrs='0.29 / W'
+ sa=0 sb=0 sd=0 mult=64 m=64
XM7 I_Bias I_Bias net1 VN sky130_fd_pr__nfet_01v8 L=0.15 W=2 nf=1 ad='int((nf+1)/2) * W/nf * 0.29' as='int((nf+2)/2) * W/nf * 0.29'
+ pd='2*int((nf+1)/2) * (W/nf + 0.29)' ps='2*int((nf+2)/2) * (W/nf + 0.29)' nrd='0.29 / W' nrs='0.29 / W'
+ sa=0 sb=0 sd=0 mult=2 m=2
XM8 net1 I_Bias VN VN sky130_fd_pr__nfet_01v8 L=0.5 W=2 nf=1 ad='int((nf+1)/2) * W/nf * 0.29' as='int((nf+2)/2) * W/nf * 0.29'
+ pd='2*int((nf+1)/2) * (W/nf + 0.29)' ps='2*int((nf+2)/2) * (W/nf + 0.29)' nrd='0.29 / W' nrs='0.29 / W'
+ sa=0 sb=0 sd=0 mult=2*2 m=2*2
XM2 V_da2_P V_da1_P VM1_D VM1_D sky130_fd_pr__nfet_01v8_lvt L=0.15 W=2 nf=1 ad='int((nf+1)/2) * W/nf * 0.29'
+ as='int((nf+2)/2) * W/nf * 0.29' pd='2*int((nf+1)/2) * (W/nf + 0.29)' ps='2*int((nf+2)/2) * (W/nf + 0.29)'
+ nrd='0.29 / W' nrs='0.29 / W' sa=0 sb=0 sd=0 mult=44*2 m=44*2
XM4 V_da2_N V_da1_N VM1_D VM1_D sky130_fd_pr__nfet_01v8_lvt L=0.15 W=2 nf=1 ad='int((nf+1)/2) * W/nf * 0.29'
+ as='int((nf+2)/2) * W/nf * 0.29' pd='2*int((nf+1)/2) * (W/nf + 0.29)' ps='2*int((nf+2)/2) * (W/nf + 0.29)'
+ nrd='0.29 / W' nrs='0.29 / W' sa=0 sb=0 sd=0 mult=44*2 m=44*2
XM9 net2 I_Bias net5 VN sky130_fd_pr__nfet_01v8 L=0.5 W=2 nf=1 ad='int((nf+1)/2) * W/nf * 0.29' as='int((nf+2)/2) * W/nf * 0.29'
+ pd='2*int((nf+1)/2) * (W/nf + 0.29)' ps='2*int((nf+2)/2) * (W/nf + 0.29)' nrd='0.29 / W' nrs='0.29 / W'
+ sa=0 sb=0 sd=0 mult=2*(256+64) m=2*(256+64)
XM10 VM1_D I_Bias net2 VN sky130_fd_pr__nfet_01v8 L=0.15 W=2 nf=1 ad='int((nf+1)/2) * W/nf * 0.29' as='int((nf+2)/2) * W/nf * 0.29'
+ pd='2*int((nf+1)/2) * (W/nf + 0.29)' ps='2*int((nf+2)/2) * (W/nf + 0.29)' nrd='0.29 / W' nrs='0.29 / W'
+ sa=0 sb=0 sd=0 mult=256+64 m=256+64
XM11 OutputP V_da2_P VM14D VM14D sky130_fd_pr__nfet_01v8_lvt L=0.15 W=2 nf=1 ad='int((nf+1)/2) * W/nf * 0.29'
+ as='int((nf+2)/2) * W/nf * 0.29' pd='2*int((nf+1)/2) * (W/nf + 0.29)' ps='2*int((nf+2)/2) * (W/nf + 0.29)'
+ nrd='0.29 / W' nrs='0.29 / W' sa=0 sb=0 sd=0 mult=44*4*2 m=44*4*2
XM12 OutputN V_da2_N VM14D VM14D sky130_fd_pr__nfet_01v8_lvt L=0.15 W=2 nf=1 ad='int((nf+1)/2) * W/nf * 0.29'
+ as='int((nf+2)/2) * W/nf * 0.29' pd='2*int((nf+1)/2) * (W/nf + 0.29)' ps='2*int((nf+2)/2) * (W/nf + 0.29)'
+ nrd='0.29 / W' nrs='0.29 / W' sa=0 sb=0 sd=0 mult=44*4*2 m=44*4*2
XM13 net3 I_Bias net6 VN sky130_fd_pr__nfet_01v8 L=0.5 W=2 nf=1 ad='int((nf+1)/2) * W/nf * 0.29' as='int((nf+2)/2) * W/nf * 0.29'
+ pd='2*int((nf+1)/2) * (W/nf + 0.29)' ps='2*int((nf+2)/2) * (W/nf + 0.29)' nrd='0.29 / W' nrs='0.29 / W'
+ sa=0 sb=0 sd=0 mult=2*(1024+256) m=2*(1024+256)
XM14 VM14D I_Bias net3 VN sky130_fd_pr__nfet_01v8 L=0.15 W=2 nf=1 ad='int((nf+1)/2) * W/nf * 0.29' as='int((nf+2)/2) * W/nf * 0.29'
+ pd='2*int((nf+1)/2) * (W/nf + 0.29)' ps='2*int((nf+2)/2) * (W/nf + 0.29)' nrd='0.29 / W' nrs='0.29 / W'
+ sa=0 sb=0 sd=0 mult=1024+256 m=1024+256
XR7 V_da2_N VP VP sky130_fd_pr__res_high_po_5p73 L=4 mult=4*2 m=4*2
XR5 V_da2_P VP VP sky130_fd_pr__res_high_po_5p73 L=4 mult=4*2 m=4*2
XR3 V_da1_N VP VP sky130_fd_pr__res_high_po_2p85 L=6 mult=4 m=4
XR4 V_da1_P VP VP sky130_fd_pr__res_high_po_2p85 L=6 mult=4 m=4
XC2 InputRef VN sky130_fd_pr__cap_mim_m3_2 W=30 L=30 MF=1 m=1
XM5 V_da1_N InputRef VM6D VM6D sky130_fd_pr__nfet_01v8_lvt L=0.15 W=2 nf=1 ad='int((nf+1)/2) * W/nf * 0.29'
+ as='int((nf+2)/2) * W/nf * 0.29' pd='2*int((nf+1)/2) * (W/nf + 0.29)' ps='2*int((nf+2)/2) * (W/nf + 0.29)'
+ nrd='0.29 / W' nrs='0.29 / W' sa=0 sb=0 sd=0 mult=11*2 m=11*2
XR8 OutputP VP VP sky130_fd_pr__res_high_po_5p73 L=4 mult=16*2 m=16*2
XC1 InputRef VN sky130_fd_pr__cap_mim_m3_2 W=30 L=30 MF=1 m=1
XC6 VP VN sky130_fd_pr__cap_mim_m3_2 W=30 L=30 MF=1 m=1
XC8 VP VN sky130_fd_pr__cap_mim_m3_2 W=30 L=30 MF=1 m=1
V1 net4 VN 0
V2 net5 VN 0
V3 net6 VN 0
XR1 OutputN VP VP sky130_fd_pr__res_high_po_5p73 L=4 mult=16*2 m=16*2
XC7 VP VN sky130_fd_pr__cap_mim_m3_2 W=30 L=30 MF=1 m=1
XC9 VP VN sky130_fd_pr__cap_mim_m3_2 W=30 L=30 MF=1 m=1
XC10 VP VN sky130_fd_pr__cap_mim_m3_2 W=30 L=30 MF=1 m=1
XC11 VP VN sky130_fd_pr__cap_mim_m3_2 W=30 L=30 MF=1 m=1
XC12 VP VN sky130_fd_pr__cap_mim_m3_2 W=30 L=30 MF=1 m=1
XC13 VP VN sky130_fd_pr__cap_mim_m3_2 W=30 L=30 MF=1 m=1
XC14 VP VN sky130_fd_pr__cap_mim_m3_2 W=30 L=30 MF=1 m=1
XC5 I_Bias VN sky130_fd_pr__cap_mim_m3_1 W=20 L=20 MF=1 m=1
XC3 I_Bias VN sky130_fd_pr__cap_mim_m3_1 W=20 L=20 MF=1 m=1
.ends


* expanding   symbol:  /home/simon/code/asic/analog/tia/tia_rgc_core.sym # of pins=8
** sym_path: xschem/tia/tia_rgc_core.sym
** sch_path: xschem/tia/tia_rgc_core.sch
.subckt tia_rgc_core VP Out_2 Out_ref Out_1 Disable_TIA Input I_Bias1 VN
*.iopin VN
*.iopin VP
*.opin Out_2
*.ipin I_Bias1
*.ipin Input
*.ipin Disable_TIA
*.opin Out_1
*.opin Out_ref
XM5 VM5D I_Bias1 VN VN sky130_fd_pr__nfet_01v8 L=1 W=2 nf=1 ad='int((nf+1)/2) * W/nf * 0.29' as='int((nf+2)/2) * W/nf * 0.29'
+ pd='2*int((nf+1)/2) * (W/nf + 0.29)' ps='2*int((nf+2)/2) * (W/nf + 0.29)' nrd='0.29 / W' nrs='0.29 / W'
+ sa=0 sb=0 sd=0 mult=6 m=6
XM6 VM6D I_Bias1 VN VN sky130_fd_pr__nfet_01v8 L=1.0 W=2 nf=1 ad='int((nf+1)/2) * W/nf * 0.29' as='int((nf+2)/2) * W/nf * 0.29'
+ pd='2*int((nf+1)/2) * (W/nf + 0.29)' ps='2*int((nf+2)/2) * (W/nf + 0.29)' nrd='0.29 / W' nrs='0.29 / W'
+ sa=0 sb=0 sd=0 mult=6 m=6
XM7 Out_1 Input VM28D VN sky130_fd_pr__nfet_01v8_lvt L=0.2 W=2 nf=1 ad='int((nf+1)/2) * W/nf * 0.29'
+ as='int((nf+2)/2) * W/nf * 0.29' pd='2*int((nf+1)/2) * (W/nf + 0.29)' ps='2*int((nf+2)/2) * (W/nf + 0.29)'
+ nrd='0.29 / W' nrs='0.29 / W' sa=0 sb=0 sd=0 mult=100 m=100
XM8 Out_1 Input VP VP sky130_fd_pr__pfet_01v8 L=0.2 W=2 nf=1 ad='int((nf+1)/2) * W/nf * 0.29' as='int((nf+2)/2) * W/nf * 0.29'
+ pd='2*int((nf+1)/2) * (W/nf + 0.29)' ps='2*int((nf+2)/2) * (W/nf + 0.29)' nrd='0.29 / W' nrs='0.29 / W'
+ sa=0 sb=0 sd=0 mult=60 m=60
XM9 Input I_Bias1 VM5D VN sky130_fd_pr__nfet_01v8 L=0.15 W=2 nf=1 ad='int((nf+1)/2) * W/nf * 0.29' as='int((nf+2)/2) * W/nf * 0.29'
+ pd='2*int((nf+1)/2) * (W/nf + 0.29)' ps='2*int((nf+2)/2) * (W/nf + 0.29)' nrd='0.29 / W' nrs='0.29 / W'
+ sa=0 sb=0 sd=0 mult=12 m=12
XM10 I_Bias1 I_Bias1 VM6D VN sky130_fd_pr__nfet_01v8 L=0.15 W=2 nf=1 ad='int((nf+1)/2) * W/nf * 0.29'
+ as='int((nf+2)/2) * W/nf * 0.29' pd='2*int((nf+1)/2) * (W/nf + 0.29)' ps='2*int((nf+2)/2) * (W/nf + 0.29)'
+ nrd='0.29 / W' nrs='0.29 / W' sa=0 sb=0 sd=0 mult=12 m=12
XM23 I_Bias1 Disable_TIA VN VN sky130_fd_pr__nfet_01v8 L=0.15 W=2 nf=1 ad='int((nf+1)/2) * W/nf * 0.29'
+ as='int((nf+2)/2) * W/nf * 0.29' pd='2*int((nf+1)/2) * (W/nf + 0.29)' ps='2*int((nf+2)/2) * (W/nf + 0.29)'
+ nrd='0.29 / W' nrs='0.29 / W' sa=0 sb=0 sd=0 mult=5 m=5
XM26 Disable_TIA_B Disable_TIA VN VN sky130_fd_pr__nfet_01v8 L=1 W=0.5 nf=1 ad='int((nf+1)/2) * W/nf * 0.29'
+ as='int((nf+2)/2) * W/nf * 0.29' pd='2*int((nf+1)/2) * (W/nf + 0.29)' ps='2*int((nf+2)/2) * (W/nf + 0.29)'
+ nrd='0.29 / W' nrs='0.29 / W' sa=0 sb=0 sd=0 mult=1 m=1
XM27 Disable_TIA_B Disable_TIA VP VP sky130_fd_pr__pfet_01v8 L=1 W=0.5 nf=1 ad='int((nf+1)/2) * W/nf * 0.29'
+ as='int((nf+2)/2) * W/nf * 0.29' pd='2*int((nf+1)/2) * (W/nf + 0.29)' ps='2*int((nf+2)/2) * (W/nf + 0.29)'
+ nrd='0.29 / W' nrs='0.29 / W' sa=0 sb=0 sd=0 mult=1 m=1
XM28 VM28D Disable_TIA_B VN VN sky130_fd_pr__nfet_01v8 L=0.15 W=2 nf=1 ad='int((nf+1)/2) * W/nf * 0.29'
+ as='int((nf+2)/2) * W/nf * 0.29' pd='2*int((nf+1)/2) * (W/nf + 0.29)' ps='2*int((nf+2)/2) * (W/nf + 0.29)'
+ nrd='0.29 / W' nrs='0.29 / W' sa=0 sb=0 sd=0 mult=100 m=100
XM36 VM36D I_Bias1 VN VN sky130_fd_pr__nfet_01v8 L=1 W=2 nf=1 ad='int((nf+1)/2) * W/nf * 0.29' as='int((nf+2)/2) * W/nf * 0.29'
+ pd='2*int((nf+1)/2) * (W/nf + 0.29)' ps='2*int((nf+2)/2) * (W/nf + 0.29)' nrd='0.29 / W' nrs='0.29 / W'
+ sa=0 sb=0 sd=0 mult=6 m=6
XM37 Out_ref VM39D VM40D VN sky130_fd_pr__nfet_01v8_lvt L=0.2 W=2 nf=1 ad='int((nf+1)/2) * W/nf * 0.29'
+ as='int((nf+2)/2) * W/nf * 0.29' pd='2*int((nf+1)/2) * (W/nf + 0.29)' ps='2*int((nf+2)/2) * (W/nf + 0.29)'
+ nrd='0.29 / W' nrs='0.29 / W' sa=0 sb=0 sd=0 mult=100 m=100
XM38 Out_ref VM39D VP VP sky130_fd_pr__pfet_01v8 L=0.2 W=2 nf=1 ad='int((nf+1)/2) * W/nf * 0.29' as='int((nf+2)/2) * W/nf * 0.29'
+ pd='2*int((nf+1)/2) * (W/nf + 0.29)' ps='2*int((nf+2)/2) * (W/nf + 0.29)' nrd='0.29 / W' nrs='0.29 / W'
+ sa=0 sb=0 sd=0 mult=60 m=60
XM39 VM39D I_Bias1 VM36D VN sky130_fd_pr__nfet_01v8 L=0.15 W=2 nf=1 ad='int((nf+1)/2) * W/nf * 0.29'
+ as='int((nf+2)/2) * W/nf * 0.29' pd='2*int((nf+1)/2) * (W/nf + 0.29)' ps='2*int((nf+2)/2) * (W/nf + 0.29)'
+ nrd='0.29 / W' nrs='0.29 / W' sa=0 sb=0 sd=0 mult=12 m=12
XM40 VM40D Disable_TIA_B VN VN sky130_fd_pr__nfet_01v8 L=0.15 W=2 nf=1 ad='int((nf+1)/2) * W/nf * 0.29'
+ as='int((nf+2)/2) * W/nf * 0.29' pd='2*int((nf+1)/2) * (W/nf + 0.29)' ps='2*int((nf+2)/2) * (W/nf + 0.29)'
+ nrd='0.29 / W' nrs='0.29 / W' sa=0 sb=0 sd=0 mult=100 m=100
XC20 VP VN sky130_fd_pr__cap_mim_m3_2 W=30 L=30 MF=1 m=1
XM16 Out_2 VN VP VP sky130_fd_pr__pfet_01v8 L=0.5 W=2 nf=1 ad='int((nf+1)/2) * W/nf * 0.29' as='int((nf+2)/2) * W/nf * 0.29'
+ pd='2*int((nf+1)/2) * (W/nf + 0.29)' ps='2*int((nf+2)/2) * (W/nf + 0.29)' nrd='0.29 / W' nrs='0.29 / W'
+ sa=0 sb=0 sd=0 mult=10 m=10
XM15 Out_2 Out_1 Input Input sky130_fd_pr__nfet_01v8_lvt L=0.2 W=2 nf=1 ad='int((nf+1)/2) * W/nf * 0.29'
+ as='int((nf+2)/2) * W/nf * 0.29' pd='2*int((nf+1)/2) * (W/nf + 0.29)' ps='2*int((nf+2)/2) * (W/nf + 0.29)'
+ nrd='0.29 / W' nrs='0.29 / W' sa=0 sb=0 sd=0 mult=30 m=30
XM31 VM31D Out_ref VM39D VM39D sky130_fd_pr__nfet_01v8_lvt L=0.2 W=2 nf=1 ad='int((nf+1)/2) * W/nf * 0.29'
+ as='int((nf+2)/2) * W/nf * 0.29' pd='2*int((nf+1)/2) * (W/nf + 0.29)' ps='2*int((nf+2)/2) * (W/nf + 0.29)'
+ nrd='0.29 / W' nrs='0.29 / W' sa=0 sb=0 sd=0 mult=30 m=30
XM35 VM31D VN VP VP sky130_fd_pr__pfet_01v8 L=0.5 W=2 nf=1 ad='int((nf+1)/2) * W/nf * 0.29' as='int((nf+2)/2) * W/nf * 0.29'
+ pd='2*int((nf+1)/2) * (W/nf + 0.29)' ps='2*int((nf+2)/2) * (W/nf + 0.29)' nrd='0.29 / W' nrs='0.29 / W'
+ sa=0 sb=0 sd=0 mult=10 m=10
XC7 VP VN sky130_fd_pr__cap_mim_m3_2 W=30 L=30 MF=1 m=1
XC2 VP VM28D sky130_fd_pr__cap_mim_m3_2 W=20 L=30 MF=1 m=1
XC5 VN I_Bias1 sky130_fd_pr__cap_mim_m3_1 W=15 L=12 MF=1 m=1
XC4 VN I_Bias1 sky130_fd_pr__cap_mim_m3_1 W=15 L=12 MF=1 m=1
XC1 VP VM40D sky130_fd_pr__cap_mim_m3_2 W=20 L=30 MF=1 m=1
XC3 Disable_TIA_B VN VN sky130_fd_pr__cap_var_lvt W=2 L=5 VM=5 m=5
.ends


* expanding   symbol:  /home/simon/code/asic/analog/esd_diodes.sym # of pins=3
** sym_path: xschem/esd/esd_diodes.sym
** sch_path: xschem/esd/esd_diodes.sch
.subckt esd_diodes VP io VN
*.iopin VP
*.iopin io
*.iopin VN
XD1 io VP sky130_fd_pr__diode_pw2nd_05v5 area=1e12 pj=4e6
XD2 VN io sky130_fd_pr__diode_pw2nd_05v5 area=1e12 pj=4e6
XD3 io VP sky130_fd_pr__diode_pw2nd_05v5 area=1e12 pj=4e6
XD4 VN io sky130_fd_pr__diode_pw2nd_05v5 area=1e12 pj=4e6
XD5 io VP sky130_fd_pr__diode_pw2nd_05v5 area=1e12 pj=4e6
XD6 VN io sky130_fd_pr__diode_pw2nd_05v5 area=1e12 pj=4e6
XD7 io VP sky130_fd_pr__diode_pw2nd_05v5 area=1e12 pj=4e6
XD8 VN io sky130_fd_pr__diode_pw2nd_05v5 area=1e12 pj=4e6
XD9 io VP sky130_fd_pr__diode_pw2nd_05v5 area=1e12 pj=4e6
XD10 VN io sky130_fd_pr__diode_pw2nd_05v5 area=1e12 pj=4e6
XD11 io VP sky130_fd_pr__diode_pw2nd_05v5 area=1e12 pj=4e6
XD12 VN io sky130_fd_pr__diode_pw2nd_05v5 area=1e12 pj=4e6
XD13 io VP sky130_fd_pr__diode_pw2nd_05v5 area=1e12 pj=4e6
XD14 VN io sky130_fd_pr__diode_pw2nd_05v5 area=1e12 pj=4e6
XD15 io VP sky130_fd_pr__diode_pw2nd_05v5 area=1e12 pj=4e6
XD16 VN io sky130_fd_pr__diode_pw2nd_05v5 area=1e12 pj=4e6
XD17 io VP sky130_fd_pr__diode_pw2nd_05v5 area=1e12 pj=4e6
XD18 VN io sky130_fd_pr__diode_pw2nd_05v5 area=1e12 pj=4e6
XD19 io VP sky130_fd_pr__diode_pw2nd_05v5 area=1e12 pj=4e6
XD20 VN io sky130_fd_pr__diode_pw2nd_05v5 area=1e12 pj=4e6
XD21 io VP sky130_fd_pr__diode_pw2nd_05v5 area=1e12 pj=4e6
XD22 VN io sky130_fd_pr__diode_pw2nd_05v5 area=1e12 pj=4e6
XD23 io VP sky130_fd_pr__diode_pw2nd_05v5 area=1e12 pj=4e6
XD24 VN io sky130_fd_pr__diode_pw2nd_05v5 area=1e12 pj=4e6
XD25 io VP sky130_fd_pr__diode_pw2nd_05v5 area=1e12 pj=4e6
XD26 VN io sky130_fd_pr__diode_pw2nd_05v5 area=1e12 pj=4e6
XD27 io VP sky130_fd_pr__diode_pw2nd_05v5 area=1e12 pj=4e6
XD28 VN io sky130_fd_pr__diode_pw2nd_05v5 area=1e12 pj=4e6
XD29 io VP sky130_fd_pr__diode_pw2nd_05v5 area=1e12 pj=4e6
XD30 VN io sky130_fd_pr__diode_pw2nd_05v5 area=1e12 pj=4e6
XD31 io VP sky130_fd_pr__diode_pw2nd_05v5 area=1e12 pj=4e6
XD32 VN io sky130_fd_pr__diode_pw2nd_05v5 area=1e12 pj=4e6
XD33 io VP sky130_fd_pr__diode_pw2nd_05v5 area=1e12 pj=4e6
XD34 VN io sky130_fd_pr__diode_pw2nd_05v5 area=1e12 pj=4e6
XD35 io VP sky130_fd_pr__diode_pw2nd_05v5 area=1e12 pj=4e6
XD36 VN io sky130_fd_pr__diode_pw2nd_05v5 area=1e12 pj=4e6
XD37 io VP sky130_fd_pr__diode_pw2nd_05v5 area=1e12 pj=4e6
XD38 VN io sky130_fd_pr__diode_pw2nd_05v5 area=1e12 pj=4e6
XD39 io VP sky130_fd_pr__diode_pw2nd_05v5 area=1e12 pj=4e6
XD40 VN io sky130_fd_pr__diode_pw2nd_05v5 area=1e12 pj=4e6
.ends

.GLOBAL GND
.GLOBAL VDD
.end
